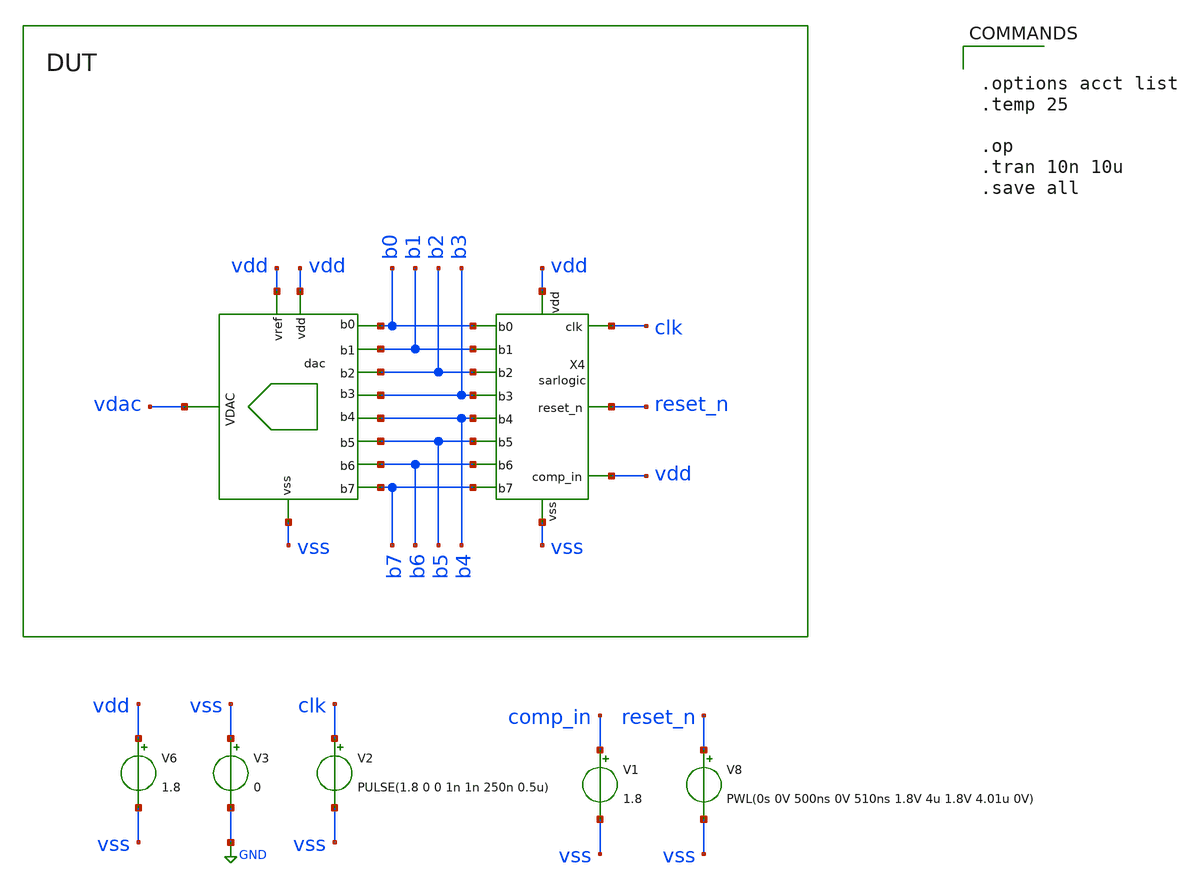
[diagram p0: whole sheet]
** sch_path: xschem/sar_logic/sar_logic_tb.sch
.lib $::SKYWATER_MODELS/sky130.lib.spice tt
.include $::SKYWATER_STDCELLS/sky130_fd_sc_hd.spice

**.subckt sar_logic_tb
V2 clk vss PULSE(1.8 0 0 1n 1n 250n 0.5u)
V1 comp_in vss 1.8
V6 vdd vss 1.8
V3 vss GND 0
V8 reset_n vss PWL(0s 0V 500ns 0V 510ns 1.8V 4u 1.8V 4.01u 0V)
X4 b0 b1 clk reset_n vdd vdd vss b2 b3 b4 b5 b6 b7 sarlogic
X1 vss vdac vdd vdd b0 b1 b2 b3 b4 b5 b6 b7 dac
**** begin user architecture code


.options acct list
.temp 25

.op
.tran 10n 10u
.save all


**** end user architecture code
**.ends

* expanding   symbol:  xschem/sar_logic/sarlogic.sym # of pins=13
** sym_path: xschem/sar_logic/sarlogic.sym
** sch_path: xschem/sar_logic/sarlogic.sch
.subckt sarlogic b0 b1 clk reset_n comp_in vdd vss b2 b3 b4 b5 b6 b7
*.iopin vdd
*.iopin clk
*.iopin b7
*.iopin b6
*.iopin b5
*.iopin b4
*.iopin b3
*.iopin b2
*.iopin b1
*.iopin b0
*.iopin comp_in
*.iopin vss
*.iopin reset_n
x7 clk vss vdd reset_n vss vss vdd vdd df8 df8_b sky130_fd_sc_hd__dfbbp_1
x1 clk df7 reset_n vdd vss vss vdd vdd df6 df6_b sky130_fd_sc_hd__dfbbp_1
x2 clk df6 reset_n vdd vss vss vdd vdd df5 df5_b sky130_fd_sc_hd__dfbbp_1
x3 clk df5 reset_n vdd vss vss vdd vdd df4 df4_b sky130_fd_sc_hd__dfbbp_1
x4 clk df4 reset_n vdd vss vss vdd vdd df3 df3_b sky130_fd_sc_hd__dfbbp_1
x5 clk df3 reset_n vdd vss vss vdd vdd df2 df2_b sky130_fd_sc_hd__dfbbp_1
x6 clk df2 reset_n vdd vss vss vdd vdd df1 df1_b sky130_fd_sc_hd__dfbbp_1
x8 clk df1 reset_n vdd vss vss vdd vdd df0 df0_b sky130_fd_sc_hd__dfbbp_1
x9 clk df0 reset_n vdd vss vss vdd vdd df00 df00_b sky130_fd_sc_hd__dfbbp_1
x10 b7 comp_in reset_n df8_b vss vss vdd vdd b8 net2 sky130_fd_sc_hd__dfbbp_1
x11 b5 comp_in reset_n df6_b vss vss vdd vdd b6 net3 sky130_fd_sc_hd__dfbbp_1
x12 b4 comp_in reset_n df5_b vss vss vdd vdd b5 net4 sky130_fd_sc_hd__dfbbp_1
x13 b3 comp_in reset_n df4_b vss vss vdd vdd b4 net5 sky130_fd_sc_hd__dfbbp_1
x14 b2 comp_in reset_n df3_b vss vss vdd vdd b3 net6 sky130_fd_sc_hd__dfbbp_1
x15 b1 comp_in reset_n df2_b vss vss vdd vdd b2 net7 sky130_fd_sc_hd__dfbbp_1
x16 b0 comp_in reset_n df1_b vss vss vdd vdd b1 net8 sky130_fd_sc_hd__dfbbp_1
x17 net1 comp_in reset_n df0_b vss vss vdd vdd b0 net9 sky130_fd_sc_hd__dfbbp_1
x18 vss vss reset_n df00_b vss vss vdd vdd net1 net10 sky130_fd_sc_hd__dfbbp_1
x19 clk df8 reset_n vdd vss vss vdd vdd df7 df7_b sky130_fd_sc_hd__dfbbp_1
x20 b6 comp_in reset_n df7_b vss vss vdd vdd b7 net11 sky130_fd_sc_hd__dfbbp_1
.ends


* expanding   symbol:  xschem/dac/dac.sym # of pins=12
** sym_path: xschem/dac/dac.sym
** sch_path: xschem/dac/dac.sch
.subckt dac vss vdac vdd vref s0 s1 s2 s3 s4 s5 s6 s7
*.ipin s7
*.ipin s6
*.ipin s5
*.ipin s4
*.ipin s3
*.ipin s2
*.ipin s1
*.ipin s0
*.iopin vdd
*.iopin vss
*.iopin vref
*.opin vdac
XC2 vdac net1 sky130_fd_pr__cap_mim_m3_1 W=1 L=1 MF=8 m=8
X2 net1 vref vss vdd s3 vss dac_sw
XC1 vdac net2 sky130_fd_pr__cap_mim_m3_1 W=4 L=1 MF=1 m=1
X3 net2 vref vss vdd s2 vss dac_sw
X4 net3 vref vss vdd s1 vss dac_sw
X5 net4 vref vss vdd s0 vss dac_sw
XC3 vdac net3 sky130_fd_pr__cap_mim_m3_1 W=2 L=1 MF=1 m=1
XC4 vdac net4 sky130_fd_pr__cap_mim_m3_1 W=1 L=1 MF=1 m=1
XC5 vss vdac sky130_fd_pr__cap_mim_m3_1 W=1 L=1 MF=1 m=1
XC6 vdac net5 sky130_fd_pr__cap_mim_m3_1 W=1 L=1 MF=16 m=16
X1 net5 vref vss vdd s4 vss dac_sw
XC7 vdac net6 sky130_fd_pr__cap_mim_m3_1 W=1 L=1 MF=32 m=32
X6 net6 vref vss vdd s5 vss dac_sw
XC8 vdac net7 sky130_fd_pr__cap_mim_m3_1 W=1 L=1 MF=64 m=64
X7 net7 vref vss vdd s6 vss dac_sw
XC9 vdac net8 sky130_fd_pr__cap_mim_m3_1 W=1 L=1 MF=128 m=128
X8 net8 vref vss vdd s7 vss dac_sw
.ends


* expanding   symbol:  xschem/dac/dac_sw.sym # of pins=6
** sym_path: xschem/dac/dac_sw.sym
** sch_path: xschem/dac/dac_sw.sch
.subckt dac_sw c b vss vdd clk a
*.iopin vdd
*.iopin vss
*.ipin clk
*.iopin c
*.iopin a
*.iopin b
XM2 c clk b vss sky130_fd_pr__nfet_01v8 L=0.15 W=10 nf=1 ad='int((nf+1)/2) * W/nf * 0.29' as='int((nf+2)/2) * W/nf * 0.29'
+ pd='2*int((nf+1)/2) * (W/nf + 0.29)' ps='2*int((nf+2)/2) * (W/nf + 0.29)' nrd='0.29 / W' nrs='0.29 / W'
+ sa=0 sb=0 sd=0 mult=1 m=1
XM5 b net1 c vdd sky130_fd_pr__pfet_01v8 L=0.15 W=20 nf=1 ad='int((nf+1)/2) * W/nf * 0.29' as='int((nf+2)/2) * W/nf * 0.29'
+ pd='2*int((nf+1)/2) * (W/nf + 0.29)' ps='2*int((nf+2)/2) * (W/nf + 0.29)' nrd='0.29 / W' nrs='0.29 / W'
+ sa=0 sb=0 sd=0 mult=1 m=1
XM6 c net1 a vss sky130_fd_pr__nfet_01v8 L=0.15 W=10 nf=1 ad='int((nf+1)/2) * W/nf * 0.29' as='int((nf+2)/2) * W/nf * 0.29'
+ pd='2*int((nf+1)/2) * (W/nf + 0.29)' ps='2*int((nf+2)/2) * (W/nf + 0.29)' nrd='0.29 / W' nrs='0.29 / W'
+ sa=0 sb=0 sd=0 mult=1 m=1
XM7 a clk c vdd sky130_fd_pr__pfet_01v8 L=0.15 W=20 nf=1 ad='int((nf+1)/2) * W/nf * 0.29' as='int((nf+2)/2) * W/nf * 0.29'
+ pd='2*int((nf+1)/2) * (W/nf + 0.29)' ps='2*int((nf+2)/2) * (W/nf + 0.29)' nrd='0.29 / W' nrs='0.29 / W'
+ sa=0 sb=0 sd=0 mult=1 m=1
x1 clk vss vss vdd vdd net1 sky130_fd_sc_hd__inv_1
.ends

.GLOBAL GND
.end
